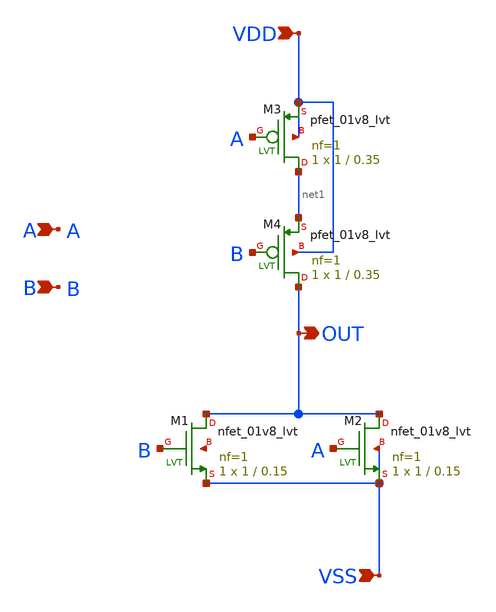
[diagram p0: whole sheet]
** sch_path: design/LELO_SVOD_SKY130A/LELO_NOR.sch
**.subckt LELO_NOR VDD VSS OUT A B
*.ipin VDD
*.ipin VSS
*.opin OUT
*.ipin A
*.ipin B
XM1 OUT B VSS net2 sky130_fd_pr__nfet_01v8_lvt L=0.15 W=1 nf=1 ad='int((1 + 1)/2) * 1 / 1 * 0.29' as='int((1 + 2)/2) * 1 / 1 * 0.29'
+ pd='2*int((1 + 1)/2) * (1 / 1 + 0.29)' ps='2*int((1 + 2)/2) * (1 / 1 + 0.29)' nrd='0.29 / 1 ' nrs='0.29 / 1 '
+ sa=0 sb=0 sd=0 mult=1 m=1
XM2 OUT A VSS VSS sky130_fd_pr__nfet_01v8_lvt L=0.15 W=1 nf=1 ad='int((1 + 1)/2) * 1 / 1 * 0.29' as='int((1 + 2)/2) * 1 / 1 * 0.29'
+ pd='2*int((1 + 1)/2) * (1 / 1 + 0.29)' ps='2*int((1 + 2)/2) * (1 / 1 + 0.29)' nrd='0.29 / 1 ' nrs='0.29 / 1 '
+ sa=0 sb=0 sd=0 mult=1 m=1
XM3 net1 A VDD VDD sky130_fd_pr__pfet_01v8_lvt L=0.35 W=1 nf=1 ad='int((1 + 1)/2) * 1 / 1 * 0.29' as='int((1 + 2)/2) * 1 / 1 * 0.29'
+ pd='2*int((1 + 1)/2) * (1 / 1 + 0.29)' ps='2*int((1 + 2)/2) * (1 / 1 + 0.29)' nrd='0.29 / 1 ' nrs='0.29 / 1 '
+ sa=0 sb=0 sd=0 mult=1 m=1
XM4 OUT B net1 VDD sky130_fd_pr__pfet_01v8_lvt L=0.35 W=1 nf=1 ad='int((1 + 1)/2) * 1 / 1 * 0.29' as='int((1 + 2)/2) * 1 / 1 * 0.29'
+ pd='2*int((1 + 1)/2) * (1 / 1 + 0.29)' ps='2*int((1 + 2)/2) * (1 / 1 + 0.29)' nrd='0.29 / 1 ' nrs='0.29 / 1 '
+ sa=0 sb=0 sd=0 mult=1 m=1
**.ends
.end
